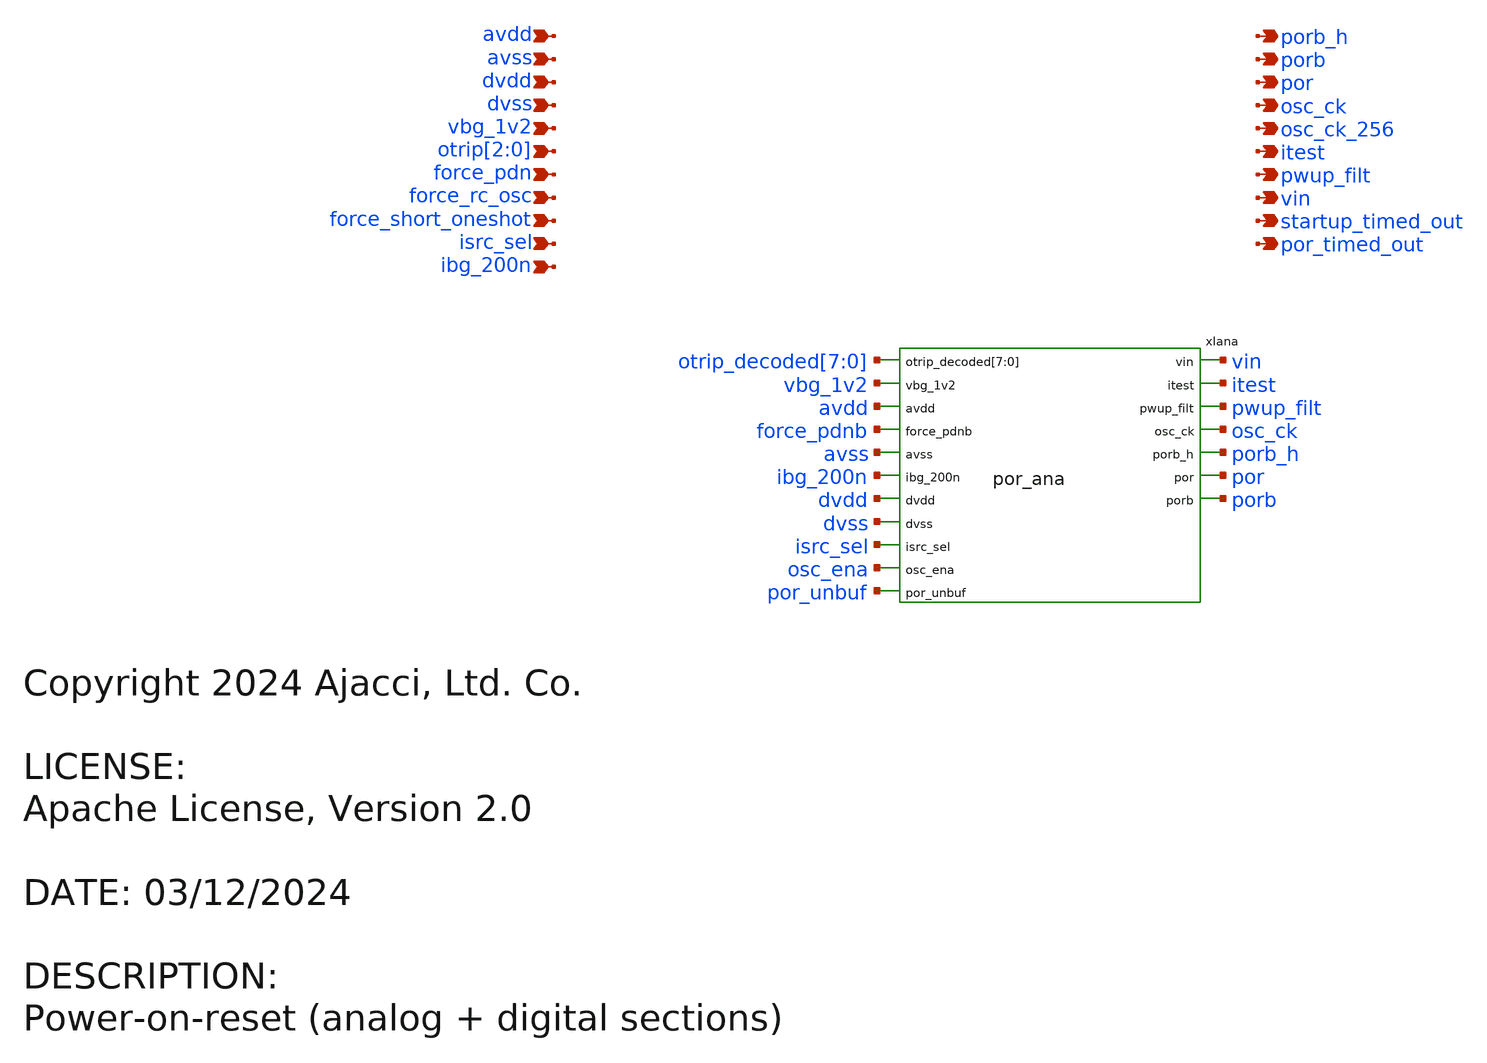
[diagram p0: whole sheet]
** sch_path: xschem/por.sch
* Copyright 2024 Ajacci, Ltd. Co.
* LICENSE:
* Apache License, Version 2.0
**.subckt por avdd avss dvdd dvss vbg_1v2 otrip[2],otrip[1],otrip[0] force_pdn force_rc_osc
*+ force_short_oneshot isrc_sel ibg_200n vin porb_h porb por osc_ck osc_ck_256 pwup_filt itest startup_timed_out
*+ por_timed_out
*.ipin avdd
*.ipin avss
*.ipin dvdd
*.ipin dvss
*.ipin vbg_1v2
*.ipin otrip[2],otrip[1],otrip[0]
*.ipin force_pdn
*.ipin force_rc_osc
*.ipin force_short_oneshot
*.ipin isrc_sel
*.ipin ibg_200n
*.opin vin
*.opin porb_h
*.opin porb
*.opin por
*.opin osc_ck
*.opin osc_ck_256
*.opin pwup_filt
*.opin itest
*.opin startup_timed_out
*.opin por_timed_out
xIana otrip_decoded[7] otrip_decoded[6] otrip_decoded[5] otrip_decoded[4] otrip_decoded[3]
+ otrip_decoded[2] otrip_decoded[1] otrip_decoded[0] vin vbg_1v2 avdd itest force_pdnb avss ibg_200n dvdd dvss
+ isrc_sel pwup_filt osc_ck osc_ena porb_h por_unbuf por porb por_ana
**** begin user architecture code



*XSPICE CO-SIM netlist
.include por_dig.out.spice
xipor_dig dvss dvdd force_pdn force_pdnb force_rc_osc force_short_oneshot osc_ck osc_ck_256 osc_ena
+  otrip_0_ otrip_1_ otrip_2_ otrip_decoded_0_ otrip_decoded_1_ otrip_decoded_2_ otrip_decoded_3_
+ otrip_decoded_4_ otrip_decoded_5_ otrip_decoded_6_ otrip_decoded_7_ por_timed_out por_unbuf pwup_filt
+ startup_timed_out por_dig


**** end user architecture code
**.ends
.end
